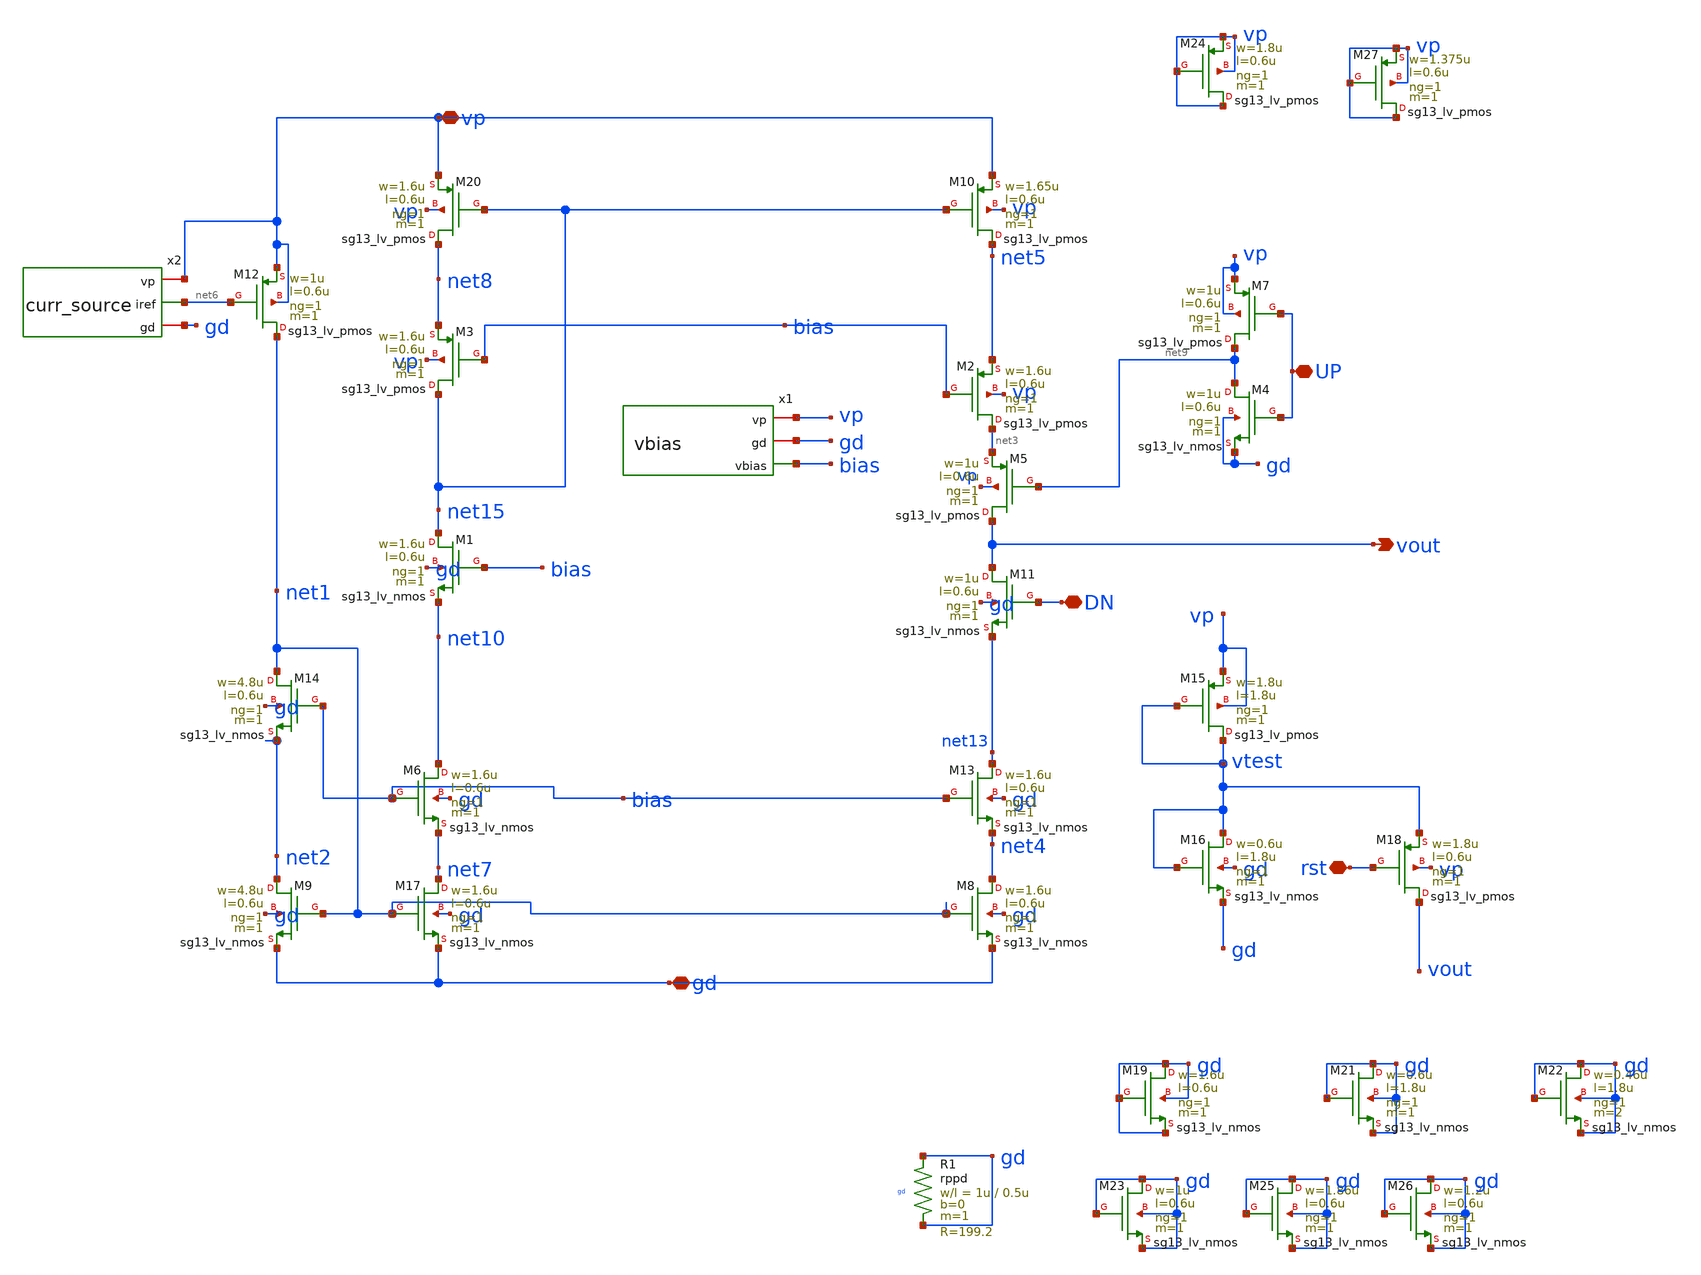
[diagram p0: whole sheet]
** sch_path: PLL0663-main/schematic/xschem/charge_pump/charge_pump_cell.sch
**.subckt charge_pump_cell UP DN gd vp vout rst
*.iopin UP
*.iopin DN
*.iopin gd
*.iopin vp
*.opin vout
*.iopin rst
x1 vp gd bias vbias
x2 vp net6 gd curr_source
XM20 net8 net15 vp vp sg13_lv_pmos w=1.6u l=0.6u ng=1 m=1 mm_ok=1
XM3 net15 bias net8 vp sg13_lv_pmos w=1.6u l=0.6u ng=1 m=1 mm_ok=1
XM12 net1 net6 vp vp sg13_lv_pmos w=1u l=0.6u ng=1 m=1 mm_ok=1
XM14 net1 bias net2 gd sg13_lv_nmos w=4.8u l=0.6u ng=1 m=1 mm_ok=1
XM9 net2 net1 gd gd sg13_lv_nmos w=4.8u l=0.6u ng=1 m=1 mm_ok=1
XM17 net7 net1 gd gd sg13_lv_nmos w=1.6u l=0.6u ng=1 m=1 mm_ok=1
XM6 net10 bias net7 gd sg13_lv_nmos w=1.6u l=0.6u ng=1 m=1 mm_ok=1
XM10 net5 net15 vp vp sg13_lv_pmos w=1.65u l=0.6u ng=1 m=1 mm_ok=1
XM2 net3 bias net5 vp sg13_lv_pmos w=1.6u l=0.6u ng=1 m=1 mm_ok=1
XM5 vout net9 net3 vp sg13_lv_pmos w=1u l=0.6u ng=1 m=1 mm_ok=1
XM7 net9 UP vp vp sg13_lv_pmos w=1u l=0.6u ng=1 m=1 mm_ok=1
XM4 net9 UP gd gd sg13_lv_nmos w=1u l=0.6u ng=1 m=1 mm_ok=1
XM11 vout DN net13 gd sg13_lv_nmos w=1u l=0.6u ng=1 m=1 mm_ok=1
XM13 net13 bias net4 gd sg13_lv_nmos w=1.6u l=0.6u ng=1 m=1 mm_ok=1
XM8 net4 net1 gd gd sg13_lv_nmos w=1.6u l=0.6u ng=1 m=1 mm_ok=1
XM15 vtest vtest vp vp sg13_lv_pmos w=1.8u l=1.8u ng=1 m=1 mm_ok=1
XM16 vtest vtest gd gd sg13_lv_nmos w=0.6u l=1.8u ng=1 m=1 mm_ok=1
XM18 vout rst vtest vp sg13_lv_pmos w=1.8u l=0.6u ng=1 m=1 mm_ok=1
XM1 net15 bias net10 gd sg13_lv_nmos w=1.6u l=0.6u ng=1 m=1 mm_ok=1
XM19 gd gd gd gd sg13_lv_nmos w=1.6u l=0.6u ng=1 m=1 mm_ok=1
XM21 gd gd gd gd sg13_lv_nmos w=0.6u l=1.8u ng=1 m=1 mm_ok=1
XM22 gd gd gd gd sg13_lv_nmos w=0.46u l=1.8u ng=1 m=2 mm_ok=1
XM23 gd gd gd gd sg13_lv_nmos w=1u l=0.6u ng=1 m=1 mm_ok=1
XM24 vp vp vp vp sg13_lv_pmos w=1.8u l=0.6u ng=1 m=1 mm_ok=1
XM25 gd gd gd gd sg13_lv_nmos w=1.86u l=0.6u ng=1 m=1 mm_ok=1
XM26 gd gd gd gd sg13_lv_nmos w=1.2u l=0.6u ng=1 m=1 mm_ok=1
XM27 vp vp vp vp sg13_lv_pmos w=1.375u l=0.6u ng=1 m=1 mm_ok=1
XR1 gd gd gd rppd w=1u l=0.5u m=1 b=0 mm_ok=1
**.ends

* expanding   symbol:
*+  /foss/designs/IHP__PLL0663/PLL0663-main/schematic/xschem/charge_pump/vbias.sym # of pins=3
** sym_path: /foss/designs/IHP__PLL0663/PLL0663-main/schematic/xschem/charge_pump/vbias.sym
** sch_path: /foss/designs/IHP__PLL0663/PLL0663-main/schematic/xschem/charge_pump/vbias.sch
.subckt vbias vp gd vbias
*.opin vbias
*.iopin gd
*.iopin vp
XM5 net1 iref vp vp sg13_lv_pmos w=1.2u l=0.6u ng=1 m=1 mm_ok=1
XM6 vbias net1 net2 gd sg13_lv_nmos w=3.6u l=0.6u ng=1 m=1 mm_ok=1
XM2 net2 net2 gd gd sg13_lv_nmos w=1.2u l=0.6u ng=1 m=1 mm_ok=1
XM3 gd gd gd gd sg13_lv_nmos w=1.86u l=0.6u ng=1 m=1 mm_ok=1
XM7 vp vp vp vp sg13_lv_pmos w=1.375u l=0.6u ng=1 m=1 mm_ok=1
XR1 net1 vbias gd rppd w=1e-6 l=1.7e-6 m=1 b=0 mm_ok=1
x1 vp iref gd curr_source
.ends


* expanding   symbol:
*+  /foss/designs/IHP__PLL0663/PLL0663-main/schematic/xschem/charge_pump/curr_source.sym # of pins=3
** sym_path: /foss/designs/IHP__PLL0663/PLL0663-main/schematic/xschem/charge_pump/curr_source.sym
** sch_path: /foss/designs/IHP__PLL0663/PLL0663-main/schematic/xschem/charge_pump/curr_source.sch
.subckt curr_source vp iref gd
*.iopin vp
*.iopin gd
*.opin iref
XM9 net3 net3 gd gd sg13_lv_nmos w=1u l=0.6u ng=1 m=1 mm_ok=1
XM4 iref iref vp vp sg13_lv_pmos w=1.4u l=0.6u ng=1 m=1 mm_ok=1
XM5 net2 iref vp vp sg13_lv_pmos w=1.2u l=0.6u ng=1 m=1 mm_ok=1
XM10 iref net2 net1 gd sg13_lv_nmos w=1.2u l=0.6u ng=1 m=1 mm_ok=1
XM1 net2 net2 gd gd sg13_lv_nmos w=1.4u l=0.6u ng=1 m=1 mm_ok=1
XM3 vp vp net3 gd sg13_lv_nmos w=1u l=0.6u ng=1 m=1 mm_ok=1
XM6 vp net3 iref gd sg13_lv_nmos w=1u l=0.6u ng=1 m=1 mm_ok=1
XM2 gd gd gd gd sg13_lv_nmos w=0.4u l=0.6u ng=1 m=1 mm_ok=1
XR2 net1 gd gd rppd w=1e-6 l=1.7e-6 m=1 b=0 mm_ok=1
.ends

.end
